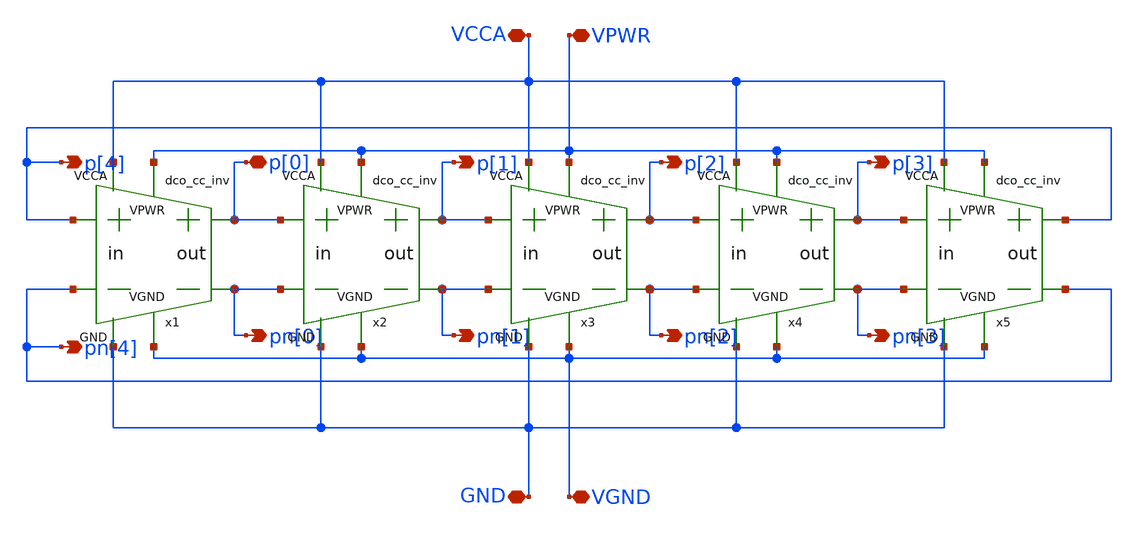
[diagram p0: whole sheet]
** sch_path: xschem/lib_dco/dco_ring_osc.sch
**.subckt dco_ring_osc VPWR VGND pn[0] p[0] pn[1] p[1] p[2] p[3] p[4] pn[2] pn[3] pn[4] VCCA GND
*.iopin VPWR
*.iopin VGND
*.opin pn[0]
*.iopin p[0]
*.opin pn[1]
*.opin p[1]
*.opin p[2]
*.opin p[3]
*.opin p[4]
*.opin pn[2]
*.opin pn[3]
*.opin pn[4]
*.iopin VCCA
*.iopin GND
x1 VCCA VPWR p[0] p[4] pn[4] pn[0] GND VGND dco_cc_inv
x2 VCCA VPWR p[1] p[0] pn[0] pn[1] GND VGND dco_cc_inv
x3 VCCA VPWR p[2] p[1] pn[1] pn[2] GND VGND dco_cc_inv
x4 VCCA VPWR p[3] p[2] pn[2] pn[3] GND VGND dco_cc_inv
x5 VCCA VPWR p[4] p[3] pn[3] pn[4] GND VGND dco_cc_inv
**.ends

* expanding   symbol:  /home/toind/work/vco_adc2/xschem/lib_dco/dco_cc_inv.sym # of pins=8
** sym_path: xschem/lib_dco/dco_cc_inv.sym
** sch_path: xschem/lib_dco/dco_cc_inv.sch
.subckt dco_cc_inv VCCA VPWR outp inp inn outn GND VGND
*.opin outp
*.ipin inn
*.iopin VGND
*.opin outn
*.ipin inp
*.iopin VPWR
*.iopin VCCA
*.iopin GND
x1 VPWR VCCA outp GND VGND inp dco_main_inv
x2 VPWR VCCA outn GND VGND inn dco_main_inv
x3 VPWR VCCA outp outn GND VGND dco_aux_inv
x4 VPWR VCCA outn outp GND VGND dco_aux_inv
.ends


* expanding   symbol:  /home/toind/work/vco_adc2/xschem/lib_dco/dco_main_inv.sym # of pins=6
** sym_path: xschem/lib_dco/dco_main_inv.sym
** sch_path: xschem/lib_dco/dco_main_inv.sch
.subckt dco_main_inv VPWR VCCA Y GND VGND A
*.iopin VPWR
*.iopin VGND
*.ipin A
*.opin Y
*.iopin VCCA
*.iopin GND
XM3 Y A VGND GND sky130_fd_pr__nfet_01v8 L=1 W=4 nf=2 ad='int((nf+1)/2) * W/nf * 0.29' as='int((nf+2)/2) * W/nf * 0.29'
+ pd='2*int((nf+1)/2) * (W/nf + 0.29)' ps='2*int((nf+2)/2) * (W/nf + 0.29)' nrd='0.29 / W' nrs='0.29 / W'
+ sa=0 sb=0 sd=0 mult=1 m=1
XM4 Y A VPWR VCCA sky130_fd_pr__pfet_01v8 L=1 W=6 nf=2 ad='int((nf+1)/2) * W/nf * 0.29' as='int((nf+2)/2) * W/nf * 0.29'
+ pd='2*int((nf+1)/2) * (W/nf + 0.29)' ps='2*int((nf+2)/2) * (W/nf + 0.29)' nrd='0.29 / W' nrs='0.29 / W'
+ sa=0 sb=0 sd=0 mult=1 m=1
.ends


* expanding   symbol:  /home/toind/work/vco_adc2/xschem/lib_dco/dco_aux_inv.sym # of pins=6
** sym_path: xschem/lib_dco/dco_aux_inv.sym
** sch_path: xschem/lib_dco/dco_aux_inv.sch
.subckt dco_aux_inv VPWR VCCA A Y GND VGND
*.iopin VPWR
*.iopin VGND
*.ipin A
*.opin Y
*.iopin VCCA
*.iopin GND
XM3 Y A VGND GND sky130_fd_pr__nfet_01v8 L=1 W=2 nf=1 ad='int((nf+1)/2) * W/nf * 0.29' as='int((nf+2)/2) * W/nf * 0.29'
+ pd='2*int((nf+1)/2) * (W/nf + 0.29)' ps='2*int((nf+2)/2) * (W/nf + 0.29)' nrd='0.29 / W' nrs='0.29 / W'
+ sa=0 sb=0 sd=0 mult=1 m=1
XM4 Y A VPWR VCCA sky130_fd_pr__pfet_01v8 L=1 W=3 nf=1 ad='int((nf+1)/2) * W/nf * 0.29' as='int((nf+2)/2) * W/nf * 0.29'
+ pd='2*int((nf+1)/2) * (W/nf + 0.29)' ps='2*int((nf+2)/2) * (W/nf + 0.29)' nrd='0.29 / W' nrs='0.29 / W'
+ sa=0 sb=0 sd=0 mult=1 m=1
.ends

.end
